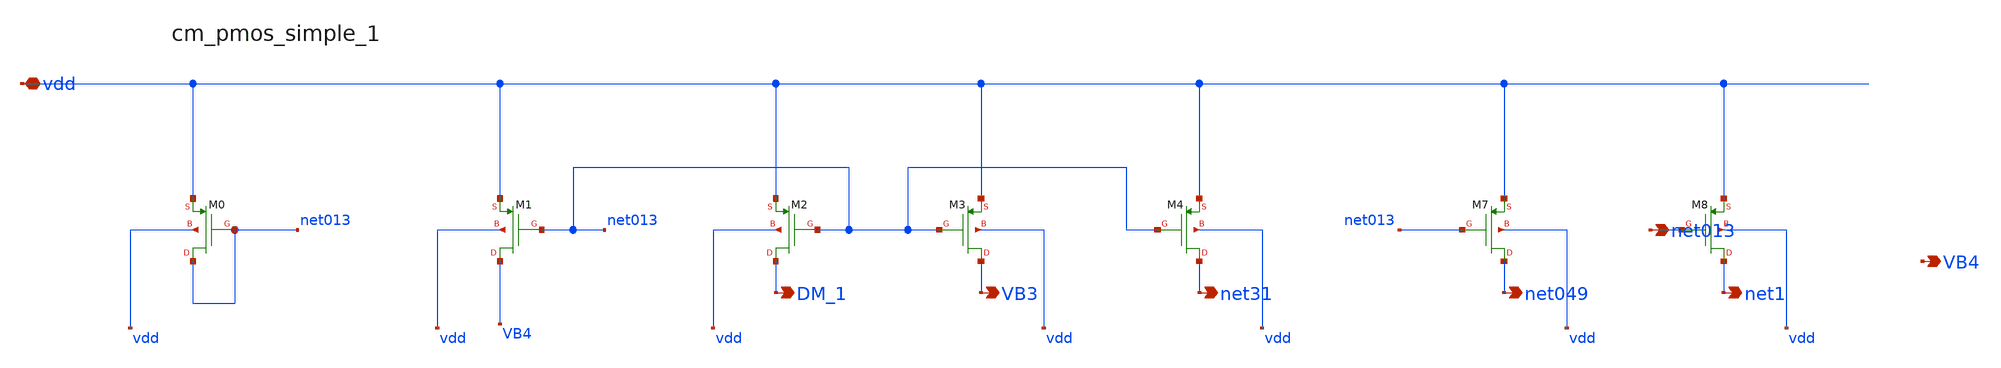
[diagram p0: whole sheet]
** sch_path: analog-db/raw/amp_010_peng_acbc/hier/blocks/cm_pmos_simple_1.sch
**.subckt cm_pmos_simple_1 vdd net013 DM_1 VB3 net31 net049 net1 VB4
*.iopin vdd
*.opin net013
*.opin DM_1
*.opin VB3
*.opin net31
*.opin net049
*.opin net1
*.opin VB4
XM0 net013 net013 vdd vdd sg13_lv_pmos w=x_dut_xm0_w l=x_dut_xm0_l ng=1 m=x_dut_xm0_m
XM1 VB4 net013 vdd vdd sg13_lv_pmos w=x_dut_xm1_w l=x_dut_xm1_l ng=1 m=x_dut_xm1_m
XM2 DM_1 net013 vdd vdd sg13_lv_pmos w=x_dut_xm2_w l=x_dut_xm2_l ng=1 m=x_dut_xm2_m
XM3 VB3 net013 vdd vdd sg13_lv_pmos w=x_dut_xm3_w l=x_dut_xm3_l ng=1 m=x_dut_xm3_m
XM4 net31 net013 vdd vdd sg13_lv_pmos w=x_dut_xm4_w l=x_dut_xm4_l ng=1 m=x_dut_xm4_m
XM7 net049 net013 vdd vdd sg13_lv_pmos w=x_dut_xm7_w l=x_dut_xm7_l ng=1 m=x_dut_xm7_m
XM8 net1 net013 vdd vdd sg13_lv_pmos w=x_dut_xm8_w l=x_dut_xm8_l ng=1 m=x_dut_xm8_m
**.ends
.end
